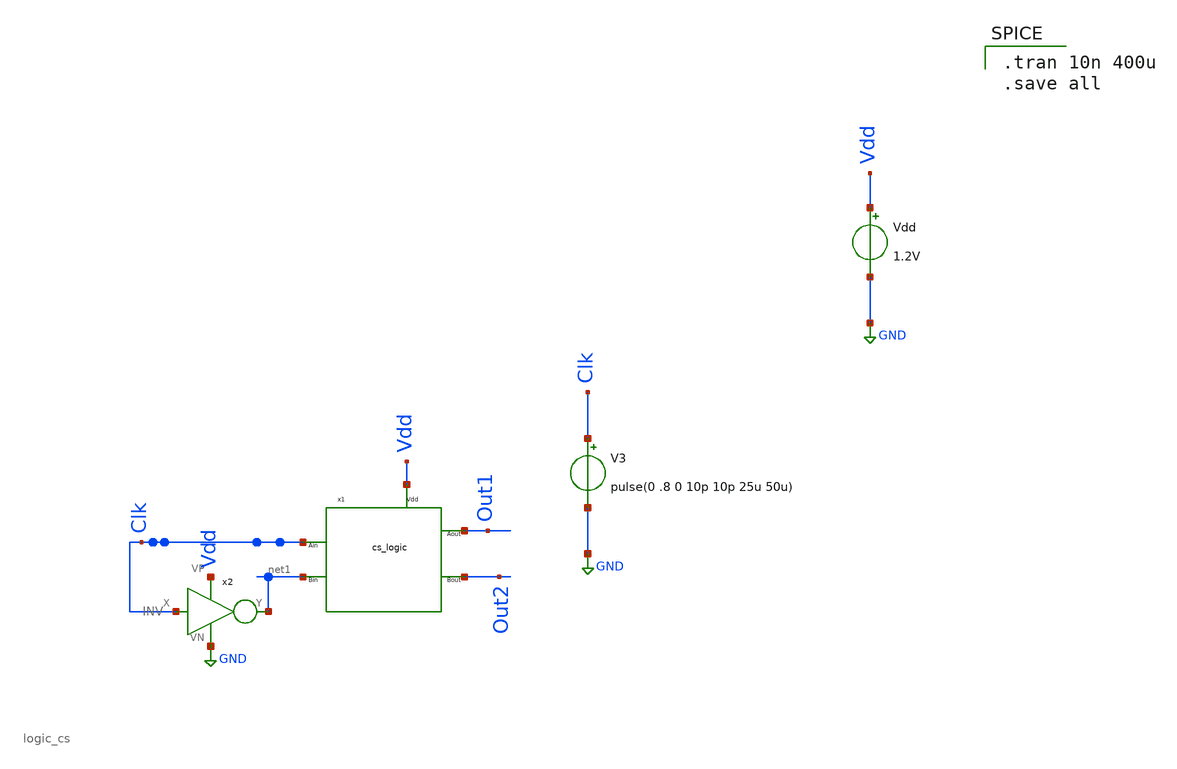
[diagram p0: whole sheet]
** sch_path: Blocks/logic_current_source/logic_cs_test.sch
**.subckt logic_cs_test
x1 Vdd Out1 Out2 net1 Clk logic_cs
Vdd Vdd GND 1.2V
V3 Clk GND pulse(0 .8 0 10p 10p 25u 50u)
x2 Clk net1 Vdd GND INV
**** begin user architecture code

** opencircuitdesign pdks install
.lib $::SKYWATER_MODELS/sky130.lib.spice tt



.tran 10n 400u
.save all

**** end user architecture code
**.ends

* expanding   symbol:  Blocks/logic_current_source/logic_cs.sym # of pins=5
** sym_path: Blocks/logic_current_source/logic_cs.sym
** sch_path: Blocks/logic_current_source/logic_cs.sch
.subckt logic_cs Vdd Aout Bout Bin Ain
*.iopin Vdd
*.iopin Aout
*.iopin Bin
*.iopin Ain
*.iopin Bout
x3 Bin net1 Aout Vdd GND NAND
x4 Ain net1 Vdd GND INV
XM1 Bout Bin GND GND sky130_fd_pr__nfet_01v8 L=0.15 W=0.42 nf=1 ad='int((nf+1)/2) * W/nf * 0.29' as='int((nf+2)/2) * W/nf * 0.29'
+ pd='2*int((nf+1)/2) * (W/nf + 0.29)' ps='2*int((nf+2)/2) * (W/nf + 0.29)' nrd='0.29 / W' nrs='0.29 / W'
+ sa=0 sb=0 sd=0 mult=1 m=1
XM2 Bout net1 GND GND sky130_fd_pr__nfet_01v8 L=0.15 W=0.42 nf=1 ad='int((nf+1)/2) * W/nf * 0.29' as='int((nf+2)/2) * W/nf * 0.29'
+ pd='2*int((nf+1)/2) * (W/nf + 0.29)' ps='2*int((nf+2)/2) * (W/nf + 0.29)' nrd='0.29 / W' nrs='0.29 / W'
+ sa=0 sb=0 sd=0 mult=1 m=1
XM3 Bout Bin net2 Vdd sky130_fd_pr__pfet_01v8 L=0.15 W=2.52 nf=1 ad='int((nf+1)/2) * W/nf * 0.29' as='int((nf+2)/2) * W/nf * 0.29'
+ pd='2*int((nf+1)/2) * (W/nf + 0.29)' ps='2*int((nf+2)/2) * (W/nf + 0.29)' nrd='0.29 / W' nrs='0.29 / W'
+ sa=0 sb=0 sd=0 mult=1 m=1
XM4 net2 net1 Vdd Vdd sky130_fd_pr__pfet_01v8 L=0.15 W=2.52 nf=1 ad='int((nf+1)/2) * W/nf * 0.29' as='int((nf+2)/2) * W/nf * 0.29'
+ pd='2*int((nf+1)/2) * (W/nf + 0.29)' ps='2*int((nf+2)/2) * (W/nf + 0.29)' nrd='0.29 / W' nrs='0.29 / W'
+ sa=0 sb=0 sd=0 mult=1 m=1
.ends


* expanding   symbol:  component/Inverter/INV.sym # of pins=4
** sym_path: component/Inverter/INV.sym
** sch_path: component/Inverter/INV.sch
.subckt INV X Y VP VN
*.ipin X
*.opin Y
*.iopin VN
*.iopin VP
XM8 Y X VP VP sky130_fd_pr__pfet_01v8 L=.18 W=1.512 nf=1 ad='int((nf+1)/2) * W/nf * 0.29' as='int((nf+2)/2) * W/nf * 0.29'
+ pd='2*int((nf+1)/2) * (W/nf + 0.29)' ps='2*int((nf+2)/2) * (W/nf + 0.29)' nrd='0.29 / W' nrs='0.29 / W'
+ sa=0 sb=0 sd=0 mult=1 m=1
XM4 Y X VN VN sky130_fd_pr__nfet_01v8 L=0.18 W=0.42 nf=1 ad='int((nf+1)/2) * W/nf * 0.29' as='int((nf+2)/2) * W/nf * 0.29'
+ pd='2*int((nf+1)/2) * (W/nf + 0.29)' ps='2*int((nf+2)/2) * (W/nf + 0.29)' nrd='0.29 / W' nrs='0.29 / W'
+ sa=0 sb=0 sd=0 mult=1 m=1
.ends


* expanding   symbol:  component/NAND2/NAND.sym # of pins=5
** sym_path: component/NAND2/NAND.sym
** sch_path: component/NAND2/NAND.sch
.subckt NAND B A Y VP VN
*.iopin VP
*.ipin A
*.ipin B
*.opin Y
*.iopin VN
XM1 Y A VP VP sky130_fd_pr__pfet_01v8 L=0.15 W=1.26 nf=1 ad='int((nf+1)/2) * W/nf * 0.29' as='int((nf+2)/2) * W/nf * 0.29'
+ pd='2*int((nf+1)/2) * (W/nf + 0.29)' ps='2*int((nf+2)/2) * (W/nf + 0.29)' nrd='0.29 / W' nrs='0.29 / W'
+ sa=0 sb=0 sd=0 mult=1 m=1
XM2 Y B VP VP sky130_fd_pr__pfet_01v8 L=0.15 W=1.26 nf=1 ad='int((nf+1)/2) * W/nf * 0.29' as='int((nf+2)/2) * W/nf * 0.29'
+ pd='2*int((nf+1)/2) * (W/nf + 0.29)' ps='2*int((nf+2)/2) * (W/nf + 0.29)' nrd='0.29 / W' nrs='0.29 / W'
+ sa=0 sb=0 sd=0 mult=1 m=1
XM3 Y A net1 net1 sky130_fd_pr__nfet_01v8 L=0.15 W=0.84 nf=1 ad='int((nf+1)/2) * W/nf * 0.29' as='int((nf+2)/2) * W/nf * 0.29'
+ pd='2*int((nf+1)/2) * (W/nf + 0.29)' ps='2*int((nf+2)/2) * (W/nf + 0.29)' nrd='0.29 / W' nrs='0.29 / W'
+ sa=0 sb=0 sd=0 mult=1 m=1
XM4 net1 B VN VN sky130_fd_pr__nfet_01v8 L=0.15 W=0.84 nf=1 ad='int((nf+1)/2) * W/nf * 0.29' as='int((nf+2)/2) * W/nf * 0.29'
+ pd='2*int((nf+1)/2) * (W/nf + 0.29)' ps='2*int((nf+2)/2) * (W/nf + 0.29)' nrd='0.29 / W' nrs='0.29 / W'
+ sa=0 sb=0 sd=0 mult=1 m=1
.ends

.GLOBAL GND
.end
